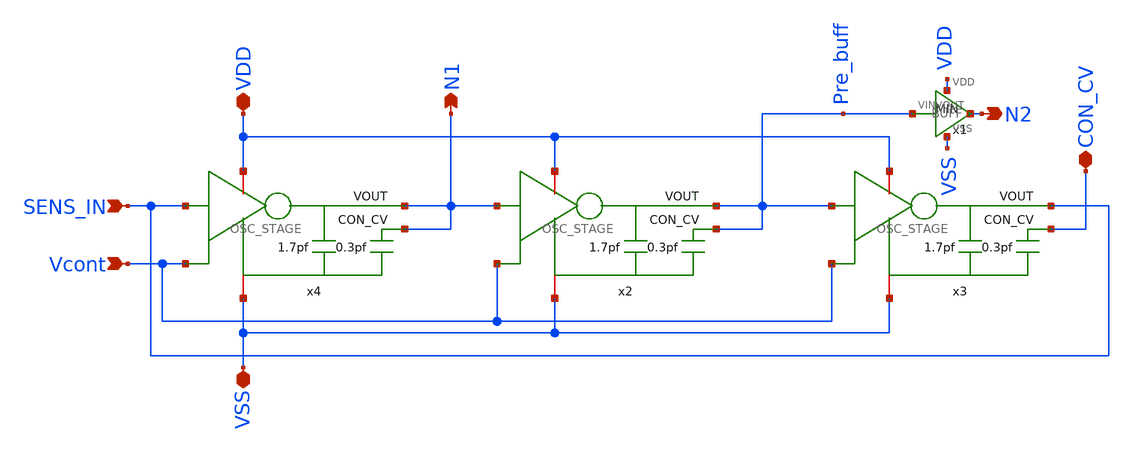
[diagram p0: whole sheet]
** sch_path: ABC123_SDC/design_data/xschem/OSC/OSC.sch
**.subckt OSC SENS_IN VDD VSS N1 N2 CON_CV Vcont
*.ipin SENS_IN
*.iopin VDD
*.iopin VSS
*.opin N1
*.opin N2
*.iopin CON_CV
*.ipin Vcont
x4 VDD N1 N1 SENS_IN VSS Vcont OSC_STAGE
x2 VDD Pre_buff Pre_buff N1 VSS Vcont OSC_STAGE
x3 VDD CON_CV SENS_IN Pre_buff VSS Vcont OSC_STAGE
x1 Pre_buff N2 VDD VSS BUFF
**.ends
.end
